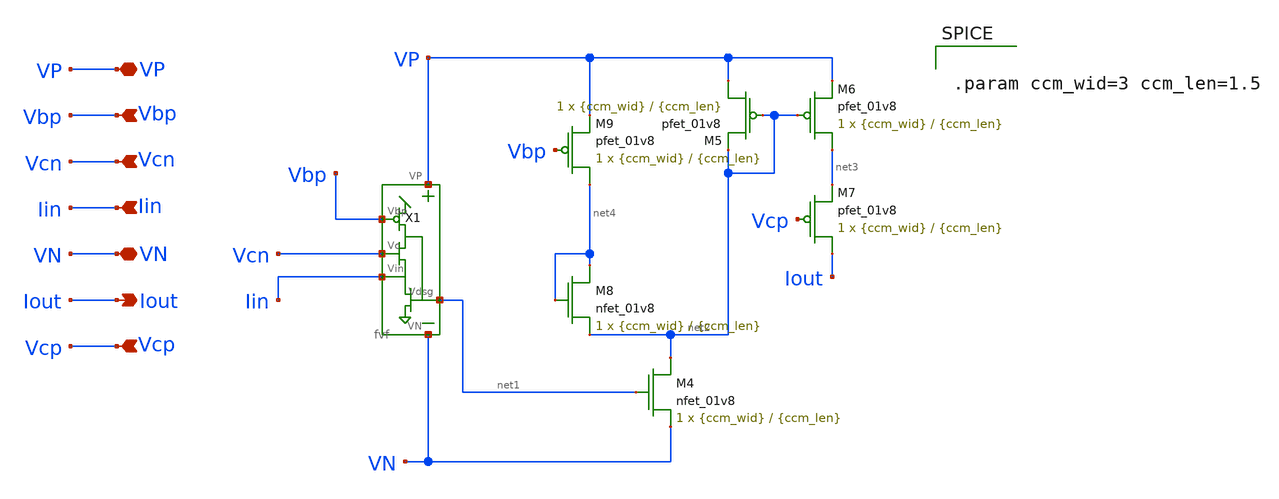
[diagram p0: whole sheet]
** sch_path: fvfccm.sch
**.subckt fvfccm Vbp Vcn Iin VP VN Iout Vcp
*.ipin Vbp
*.ipin Vcn
*.ipin Iin
*.iopin VP
*.iopin VN
*.opin Iout
*.ipin Vcp
XM4 net2 net1 VN VN sky130_fd_pr__nfet_01v8 L={ccm_len} W={ccm_wid} nf=1 ad='int((nf+1)/2) * W/nf * 0.29'
+ as='int((nf+2)/2) * W/nf * 0.29' pd='2*int((nf+1)/2) * (W/nf + 0.29)' ps='2*int((nf+2)/2) * (W/nf + 0.29)'
+ nrd='0.29 / W' nrs='0.29 / W' sa=0 sb=0 sd=0 mult=1 m=1
XM5 VP net2 net2 VP sky130_fd_pr__pfet_01v8 L={ccm_len} W={ccm_wid} nf=1 ad='int((nf+1)/2) * W/nf * 0.29'
+ as='int((nf+2)/2) * W/nf * 0.29' pd='2*int((nf+1)/2) * (W/nf + 0.29)' ps='2*int((nf+2)/2) * (W/nf + 0.29)'
+ nrd='0.29 / W' nrs='0.29 / W' sa=0 sb=0 sd=0 mult=1 m=1
XM6 net3 net2 VP VP sky130_fd_pr__pfet_01v8 L={ccm_len} W={ccm_wid} nf=1 ad='int((nf+1)/2) * W/nf * 0.29'
+ as='int((nf+2)/2) * W/nf * 0.29' pd='2*int((nf+1)/2) * (W/nf + 0.29)' ps='2*int((nf+2)/2) * (W/nf + 0.29)'
+ nrd='0.29 / W' nrs='0.29 / W' sa=0 sb=0 sd=0 mult=1 m=1
XM7 Iout Vcp net3 VP sky130_fd_pr__pfet_01v8 L={ccm_len} W={ccm_wid} nf=1 ad='int((nf+1)/2) * W/nf * 0.29'
+ as='int((nf+2)/2) * W/nf * 0.29' pd='2*int((nf+1)/2) * (W/nf + 0.29)' ps='2*int((nf+2)/2) * (W/nf + 0.29)'
+ nrd='0.29 / W' nrs='0.29 / W' sa=0 sb=0 sd=0 mult=1 m=1
XM8 net4 net4 net2 VN sky130_fd_pr__nfet_01v8 L={ccm_len} W={ccm_wid} nf=1 ad='int((nf+1)/2) * W/nf * 0.29'
+ as='int((nf+2)/2) * W/nf * 0.29' pd='2*int((nf+1)/2) * (W/nf + 0.29)' ps='2*int((nf+2)/2) * (W/nf + 0.29)'
+ nrd='0.29 / W' nrs='0.29 / W' sa=0 sb=0 sd=0 mult=1 m=1
XM9 net4 Vbp VP VP sky130_fd_pr__pfet_01v8 L={ccm_len} W={ccm_wid} nf=1 ad='int((nf+1)/2) * W/nf * 0.29'
+ as='int((nf+2)/2) * W/nf * 0.29' pd='2*int((nf+1)/2) * (W/nf + 0.29)' ps='2*int((nf+2)/2) * (W/nf + 0.29)'
+ nrd='0.29 / W' nrs='0.29 / W' sa=0 sb=0 sd=0 mult=1 m=1
X1 VP Vbp Vcn Iin net1 VN fvf
**** begin user architecture code


.param ccm_wid=3 ccm_len=1.5


**** end user architecture code
**.ends

* expanding   symbol:  fvf.sym # of pins=6
** sym_path: fvf.sym
** sch_path: fvf.sch
.subckt fvf VP Vbp Vc Vin Vdsg VN
*.iopin VP
*.ipin Vbp
*.ipin Vc
*.ipin Vin
*.iopin VN
*.opin Vdsg
XM3 Vdsg Vc Vin VN sky130_fd_pr__nfet_01v8 L={fvf_len} W={fvf_wid} nf=1 ad='int((nf+1)/2) * W/nf * 0.29'
+ as='int((nf+2)/2) * W/nf * 0.29' pd='2*int((nf+1)/2) * (W/nf + 0.29)' ps='2*int((nf+2)/2) * (W/nf + 0.29)'
+ nrd='0.29 / W' nrs='0.29 / W' sa=0 sb=0 sd=0 mult=1 m=1
XM4 VN Vdsg Vin VN sky130_fd_pr__nfet_01v8 L={fvf_len} W={fvf_wid} nf=1 ad='int((nf+1)/2) * W/nf * 0.29'
+ as='int((nf+2)/2) * W/nf * 0.29' pd='2*int((nf+1)/2) * (W/nf + 0.29)' ps='2*int((nf+2)/2) * (W/nf + 0.29)'
+ nrd='0.29 / W' nrs='0.29 / W' sa=0 sb=0 sd=0 mult=1 m=1
**** begin user architecture code


.param fvf_wid=3 fvf_len=1.5


**** end user architecture code
XM1 Vdsg Vbp VP VP sky130_fd_pr__pfet_01v8 L={fvf_len} W={fvf_wid} nf=1 ad='int((nf+1)/2) * W/nf * 0.29'
+ as='int((nf+2)/2) * W/nf * 0.29' pd='2*int((nf+1)/2) * (W/nf + 0.29)' ps='2*int((nf+2)/2) * (W/nf + 0.29)'
+ nrd='0.29 / W' nrs='0.29 / W' sa=0 sb=0 sd=0 mult=1 m=1
.ends

.end
